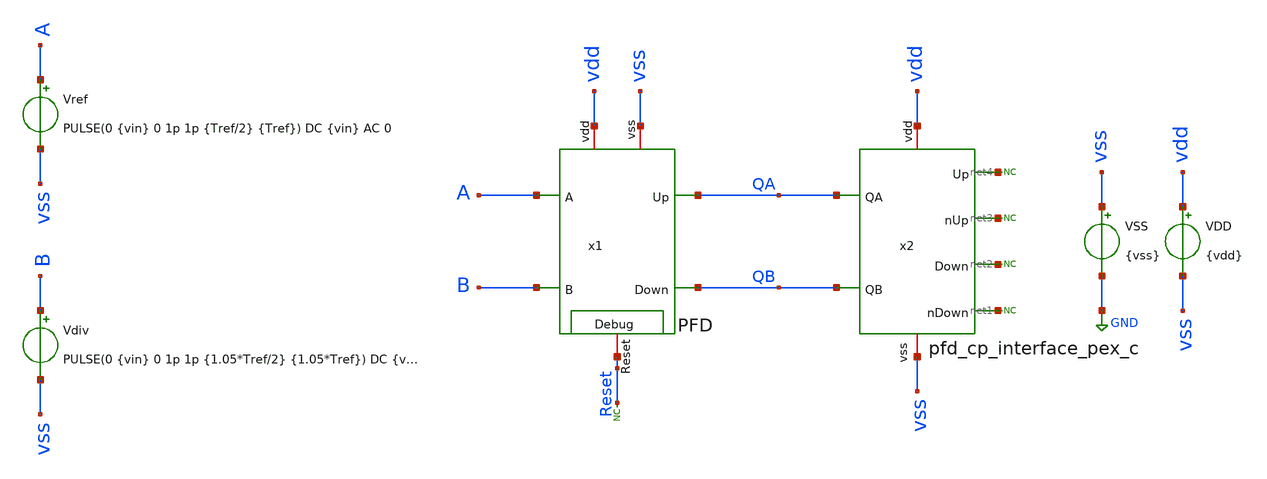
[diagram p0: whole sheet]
** sch_path: xschem/tb_PFD.sch
**.subckt tb_PFD
x1 vss vdd QA A B QB Reset PFD
VSS vss GND {vss}
VDD vdd vss {vdd}
Vref A vss PULSE(0 {vin} 0 1p 1p {Tref/2} {Tref}) DC {vin} AC 0
Vdiv B vss PULSE(0 {vin} 0 1p 1p {1.05*Tref/2} {1.05*Tref}) DC {vin} AC 0
* noconn #net1
* noconn #net2
* noconn #net3
* noconn #net4
x2 net4 vdd QA net3 net2 QB vss net1 pfd_cp_interface_pex_c
* noconn Reset
**** begin user architecture code



* Parameters
.param kp = 0.9
.param vdd = kp*1.8
.param vss = 0.0
.param vin = vdd
.param fref = 100e6
.param Tref = 1/fref
.param C = 10f

.options TEMP = 100.0

* Models
.lib ~/skywater/skywater-pdk/libraries/sky130_fd_pr_ngspice/latest/models/corners/sky130.lib SS
.include ~/caravel_analog_fulgor/xschem/simulations/pfd_cp_interface_pex_c.spice

* Data to save
.save all

.ic v(A) = 0.0
.ic v(B) = 0.0

* Simulation
.control
	tran 0.01ns 400ns
	write tb_PFD_tran.raw
 	plot v(Reset) v(QB)+2 v(QA)+4 v(A)+6 v(B)+6

.endc

.end


**** end user architecture code
**.ends

* expanding   symbol:  PFD.sym # of pins=7
** sym_path: xschem/PFD.sym
** sch_path: xschem/PFD.sch
.subckt PFD vss vdd Up A B Down Reset
*.iopin vdd
*.iopin vss
*.ipin A
*.ipin B
*.opin Down
*.opin Up
*.iopin Reset
x1 vdd A Up Reset vss DFF
x2 vdd B Down Reset vss DFF
x3 vdd Reset Up Down vss and_pfd
.ends


* expanding   symbol:  DFF.sym # of pins=5
** sym_path: xschem/DFF.sym
** sch_path: xschem/DFF.sch
.subckt DFF D CLK Q Reset vss
*.ipin D
*.ipin CLK
*.opin Q
*.ipin Reset
*.iopin vss
x1 D CLK Q P vss nor
x2 D P P1 Q vss nor
x3 D P P2 P1 vss nor
x4 D P1 Reset P2 vss nor
.ends


* expanding   symbol:  and_pfd.sym # of pins=5
** sym_path: xschem/and_pfd.sym
** sch_path: xschem/and_pfd.sch
.subckt and_pfd vdd out A B vss
*.iopin vdd
*.iopin vss
*.opin out
*.ipin A
*.ipin B
XM1 out_nand A net1 vss sky130_fd_pr__nfet_01v8 L=0.15 W=0.45 nf=1 ad='int((nf+1)/2) * W/nf * 0.29' as='int((nf+2)/2) * W/nf * 0.29'
+ pd='2*int((nf+1)/2) * (W/nf + 0.29)' ps='2*int((nf+2)/2) * (W/nf + 0.29)' nrd='0.29 / W' nrs='0.29 / W'
+ sa=0 sb=0 sd=0 mult=1 m=1
XM2 out_nand A vdd vdd sky130_fd_pr__pfet_01v8 L=0.15 W=0.9 nf=1 ad='int((nf+1)/2) * W/nf * 0.29' as='int((nf+2)/2) * W/nf * 0.29'
+ pd='2*int((nf+1)/2) * (W/nf + 0.29)' ps='2*int((nf+2)/2) * (W/nf + 0.29)' nrd='0.29 / W' nrs='0.29 / W'
+ sa=0 sb=0 sd=0 mult=1 m=1
XM3 net1 B vss vss sky130_fd_pr__nfet_01v8 L=0.15 W=0.45 nf=1 ad='int((nf+1)/2) * W/nf * 0.29' as='int((nf+2)/2) * W/nf * 0.29'
+ pd='2*int((nf+1)/2) * (W/nf + 0.29)' ps='2*int((nf+2)/2) * (W/nf + 0.29)' nrd='0.29 / W' nrs='0.29 / W'
+ sa=0 sb=0 sd=0 mult=1 m=1
XM4 out_nand B net2 vss sky130_fd_pr__nfet_01v8 L=0.15 W=0.45 nf=1 ad='int((nf+1)/2) * W/nf * 0.29' as='int((nf+2)/2) * W/nf * 0.29'
+ pd='2*int((nf+1)/2) * (W/nf + 0.29)' ps='2*int((nf+2)/2) * (W/nf + 0.29)' nrd='0.29 / W' nrs='0.29 / W'
+ sa=0 sb=0 sd=0 mult=1 m=1
XM5 net2 A vss vss sky130_fd_pr__nfet_01v8 L=0.15 W=0.45 nf=1 ad='int((nf+1)/2) * W/nf * 0.29' as='int((nf+2)/2) * W/nf * 0.29'
+ pd='2*int((nf+1)/2) * (W/nf + 0.29)' ps='2*int((nf+2)/2) * (W/nf + 0.29)' nrd='0.29 / W' nrs='0.29 / W'
+ sa=0 sb=0 sd=0 mult=1 m=1
XM6 out_nand B vdd vdd sky130_fd_pr__pfet_01v8 L=0.15 W=0.9 nf=1 ad='int((nf+1)/2) * W/nf * 0.29' as='int((nf+2)/2) * W/nf * 0.29'
+ pd='2*int((nf+1)/2) * (W/nf + 0.29)' ps='2*int((nf+2)/2) * (W/nf + 0.29)' nrd='0.29 / W' nrs='0.29 / W'
+ sa=0 sb=0 sd=0 mult=1 m=1
XM7 out out_nand vdd vdd sky130_fd_pr__pfet_01v8 L=0.15 W=0.9 nf=1 ad='int((nf+1)/2) * W/nf * 0.29' as='int((nf+2)/2) * W/nf * 0.29'
+ pd='2*int((nf+1)/2) * (W/nf + 0.29)' ps='2*int((nf+2)/2) * (W/nf + 0.29)' nrd='0.29 / W' nrs='0.29 / W'
+ sa=0 sb=0 sd=0 mult=1 m=1
XM8 out out_nand vss vss sky130_fd_pr__nfet_01v8 L=0.15 W=0.45 nf=1 ad='int((nf+1)/2) * W/nf * 0.29'
+ as='int((nf+2)/2) * W/nf * 0.29' pd='2*int((nf+1)/2) * (W/nf + 0.29)' ps='2*int((nf+2)/2) * (W/nf + 0.29)'
+ nrd='0.29 / W' nrs='0.29 / W' sa=0 sb=0 sd=0 mult=1 m=1
.ends


* expanding   symbol:  nor.sym # of pins=5
** sym_path: xschem/nor.sym
** sch_path: xschem/nor.sch
.subckt nor vdd A B out vss
*.ipin A
*.ipin B
*.iopin vdd
*.opin out
*.iopin vss
XM1 out A vss vss sky130_fd_pr__nfet_01v8 L=0.15 W=0.45 nf=1 ad='int((nf+1)/2) * W/nf * 0.29' as='int((nf+2)/2) * W/nf * 0.29'
+ pd='2*int((nf+1)/2) * (W/nf + 0.29)' ps='2*int((nf+2)/2) * (W/nf + 0.29)' nrd='0.29 / W' nrs='0.29 / W'
+ sa=0 sb=0 sd=0 mult=1 m=1
XM2 out B vss vss sky130_fd_pr__nfet_01v8 L=0.15 W=0.45 nf=1 ad='int((nf+1)/2) * W/nf * 0.29' as='int((nf+2)/2) * W/nf * 0.29'
+ pd='2*int((nf+1)/2) * (W/nf + 0.29)' ps='2*int((nf+2)/2) * (W/nf + 0.29)' nrd='0.29 / W' nrs='0.29 / W'
+ sa=0 sb=0 sd=0 mult=1 m=1
XM4 out B net1 vdd sky130_fd_pr__pfet_01v8 L=0.15 W=0.9 nf=1 ad='int((nf+1)/2) * W/nf * 0.29' as='int((nf+2)/2) * W/nf * 0.29'
+ pd='2*int((nf+1)/2) * (W/nf + 0.29)' ps='2*int((nf+2)/2) * (W/nf + 0.29)' nrd='0.29 / W' nrs='0.29 / W'
+ sa=0 sb=0 sd=0 mult=1 m=1
XM3 net1 A vdd vdd sky130_fd_pr__pfet_01v8 L=0.15 W=0.9 nf=1 ad='int((nf+1)/2) * W/nf * 0.29' as='int((nf+2)/2) * W/nf * 0.29'
+ pd='2*int((nf+1)/2) * (W/nf + 0.29)' ps='2*int((nf+2)/2) * (W/nf + 0.29)' nrd='0.29 / W' nrs='0.29 / W'
+ sa=0 sb=0 sd=0 mult=1 m=1
XM5 net2 B vdd vdd sky130_fd_pr__pfet_01v8 L=0.15 W=0.9 nf=1 ad='int((nf+1)/2) * W/nf * 0.29' as='int((nf+2)/2) * W/nf * 0.29'
+ pd='2*int((nf+1)/2) * (W/nf + 0.29)' ps='2*int((nf+2)/2) * (W/nf + 0.29)' nrd='0.29 / W' nrs='0.29 / W'
+ sa=0 sb=0 sd=0 mult=1 m=1
XM6 out A net2 vdd sky130_fd_pr__pfet_01v8 L=0.15 W=0.9 nf=1 ad='int((nf+1)/2) * W/nf * 0.29' as='int((nf+2)/2) * W/nf * 0.29'
+ pd='2*int((nf+1)/2) * (W/nf + 0.29)' ps='2*int((nf+2)/2) * (W/nf + 0.29)' nrd='0.29 / W' nrs='0.29 / W'
+ sa=0 sb=0 sd=0 mult=1 m=1
.ends

.GLOBAL GND
.end
